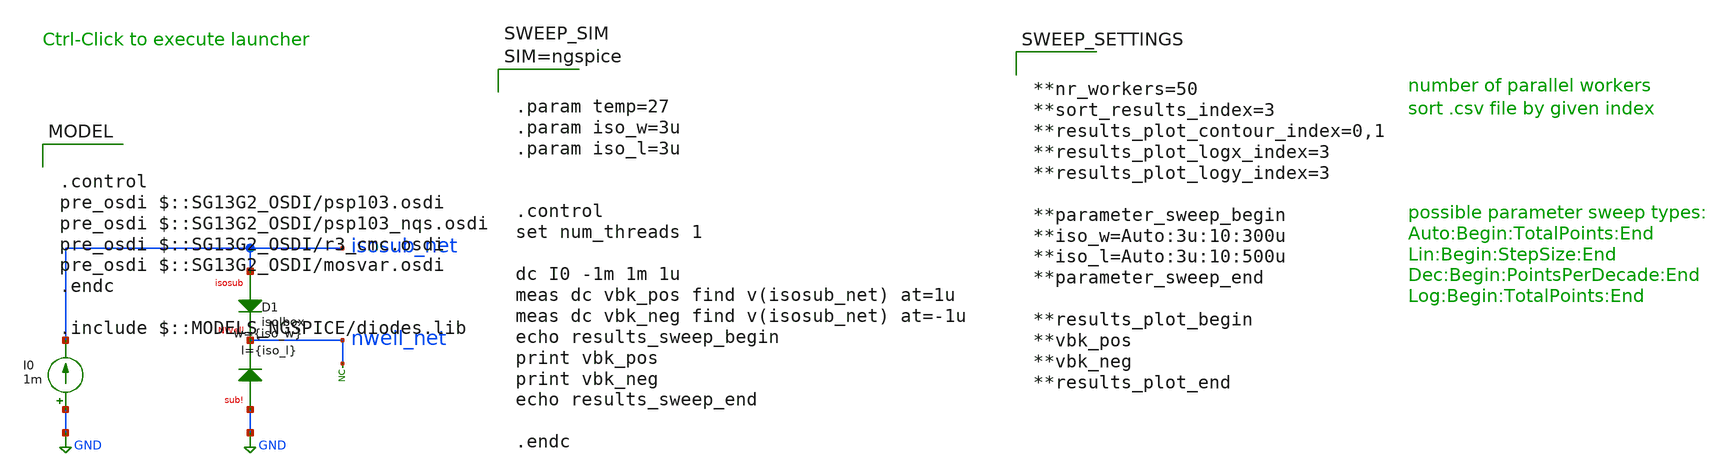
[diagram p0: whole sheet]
** sch_path: ihp-sg13g2/xschem_libs/sg13g2_tests/isolbox_sweep_tb/schematic/isolbox_sweep_tb.sch
**.subckt isolbox_sweep_tb
I0 GND isosub_net 1m
XD1 isosub_net nwell_net GND isolbox l={iso_l} w={iso_w}
* noconn nwell_net
**** begin user architecture code



.param temp=27
.param iso_w=3u
.param iso_l=3u


.control
set num_threads 1

dc I0 -1m 1m 1u
meas dc vbk_pos find v(isosub_net) at=1u
meas dc vbk_neg find v(isosub_net) at=-1u
echo results_sweep_begin
print vbk_pos
print vbk_neg
echo results_sweep_end

.endc





**nr_workers=50
**sort_results_index=3
**results_plot_contour_index=0,1
**results_plot_logx_index=3
**results_plot_logy_index=3

**parameter_sweep_begin
**iso_w=Auto:3u:10:300u
**iso_l=Auto:3u:10:500u
**parameter_sweep_end

**results_plot_begin
**vbk_pos
**vbk_neg
**results_plot_end



.control
pre_osdi $::SG13G2_OSDI/psp103.osdi
pre_osdi $::SG13G2_OSDI/psp103_nqs.osdi
pre_osdi $::SG13G2_OSDI/r3_cmc.osdi
pre_osdi $::SG13G2_OSDI/mosvar.osdi
.endc

.include $::MODELS_NGSPICE/diodes.lib

**** end user architecture code
**.ends
.GLOBAL GND
.end
